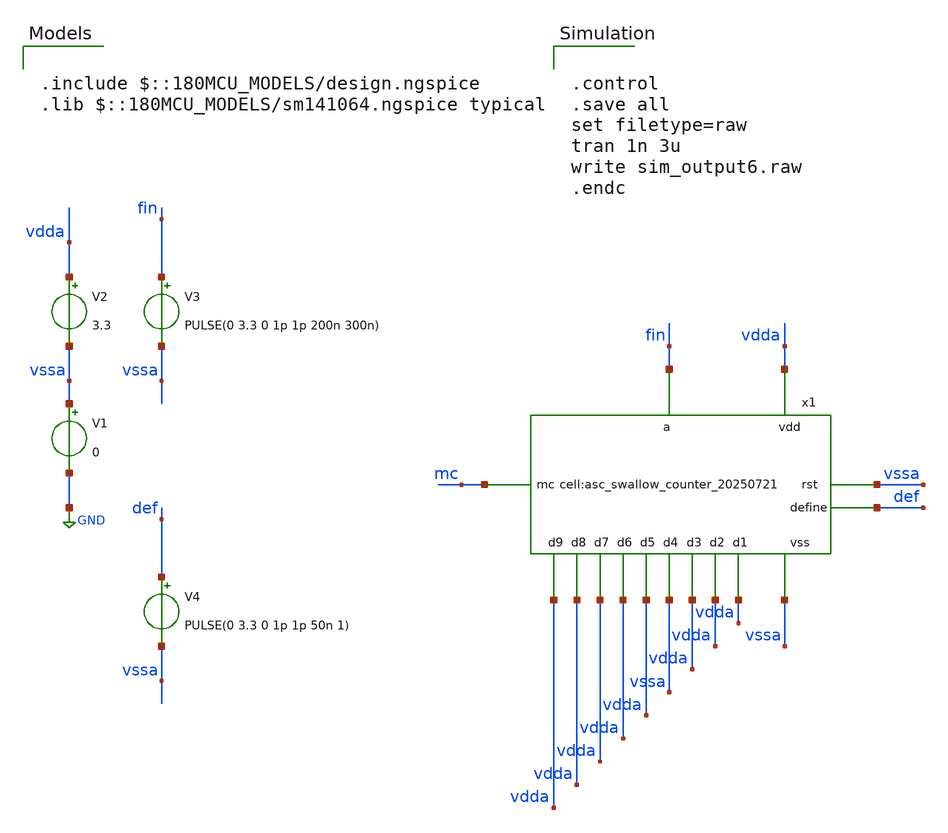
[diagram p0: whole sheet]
** sch_path: designs/libs/tb_analog/tb_asc_9_bit_counter/tb_asc_9_bit_counter.sch
**.subckt tb_asc_9_bit_counter
V1 vssa GND 0
V2 vdda vssa 3.3
V3 fin vssa PULSE(0 3.3 0 1p 1p 200n 300n)
V4 def vssa PULSE(0 3.3 0 1p 1p 50n 1)
x1 mc vdda vdda vdda vdda vdda vssa vdda vdda vdda vssa vssa vdda fin def
+ asc_swallow_counter_20250721
**** begin user architecture code

.include $::180MCU_MODELS/design.ngspice
.lib $::180MCU_MODELS/sm141064.ngspice typical



.control
.save all
set filetype=raw
tran 1n 3u
write sim_output6.raw
.endc


**** end user architecture code
**.ends
.GLOBAL GND
.end
